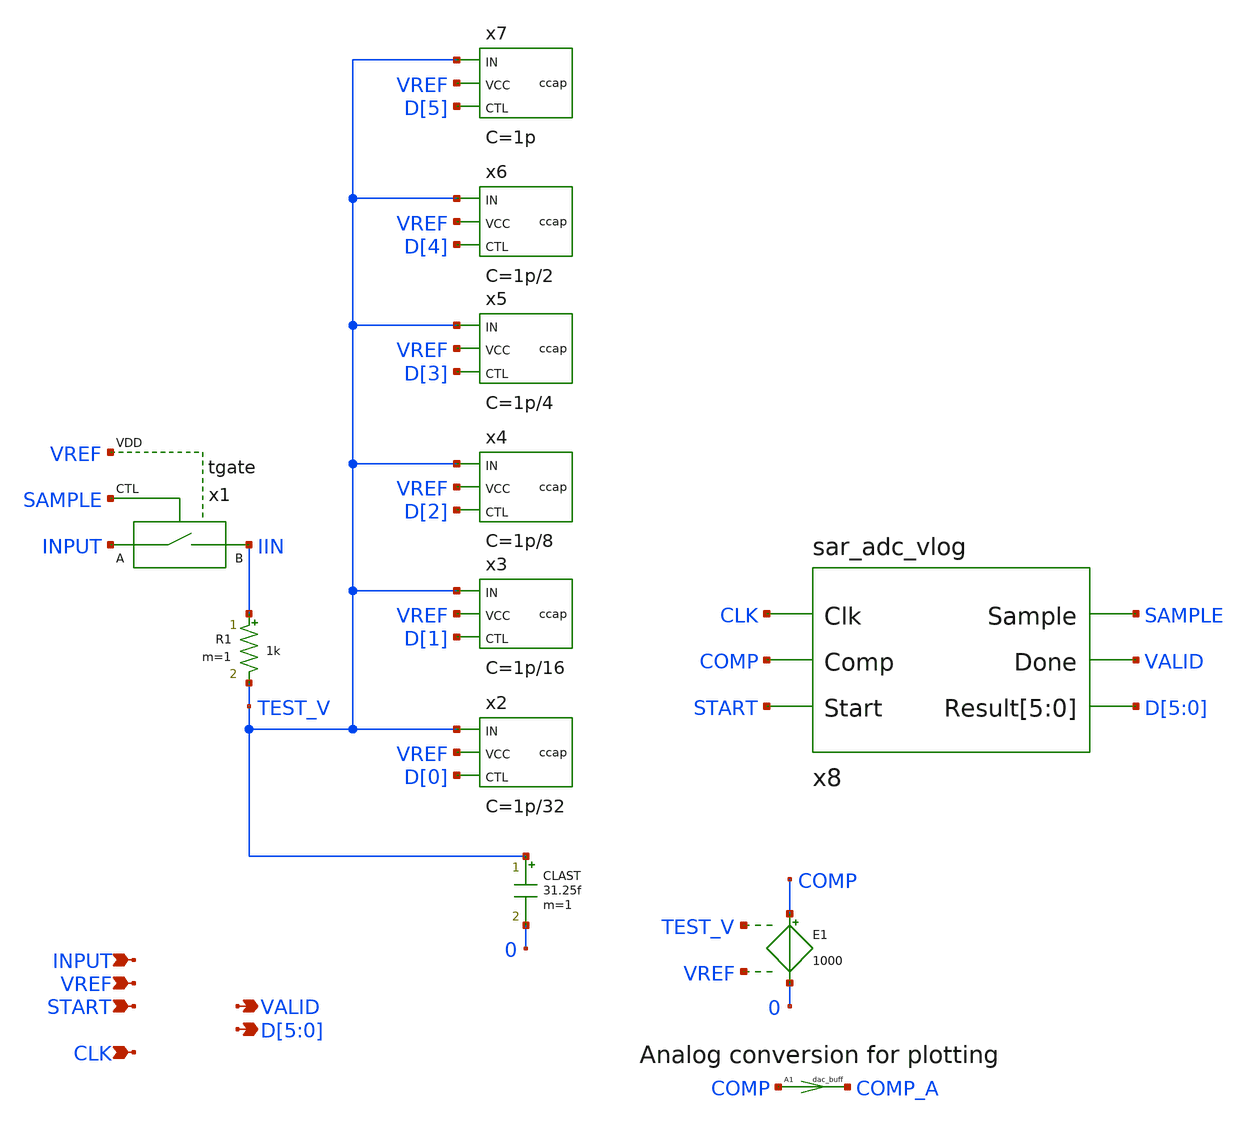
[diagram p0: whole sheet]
** sch_path: demo/cosim/test_new/vacask_cosim_hier/final_folder/sar_adc.sch
**.subckt sar_adc INPUT VREF START VALID CLK D[5],D[4],D[3],D[2],D[1],D[0]
*.ipin INPUT
*.ipin VREF
*.ipin START
*.opin VALID
*.ipin CLK
*.opin D[5],D[4],D[3],D[2],D[1],D[0]
CLAST TEST_V 0 31.25f m=1
R1 IIN TEST_V 1k m=1
A1 [ COMP ] [ COMP_A ] dac_buff
E1 COMP 0 TEST_V VREF 1000
x1 INPUT IIN SAMPLE VREF tgate
x2 TEST_V VREF D[0] ccap C = 1p/32
x3 TEST_V VREF D[1] ccap C = 1p/16
x4 TEST_V VREF D[2] ccap C = 1p/8
x5 TEST_V VREF D[3] ccap C = 1p/4
x6 TEST_V VREF D[4] ccap C = 1p/2
x7 TEST_V VREF D[5] ccap C = 1p
x8 CLK COMP VALID D[5] D[4] D[3] D[2] D[1] D[0] SAMPLE START sar_adc_vlog
**.ends
**** begin user architecture code
.model dac_buff dac_bridge input_load=1e-15 t_rise=10n t_fall=10n  out_low=0 out_high=3.3
**** end user architecture code
.end
